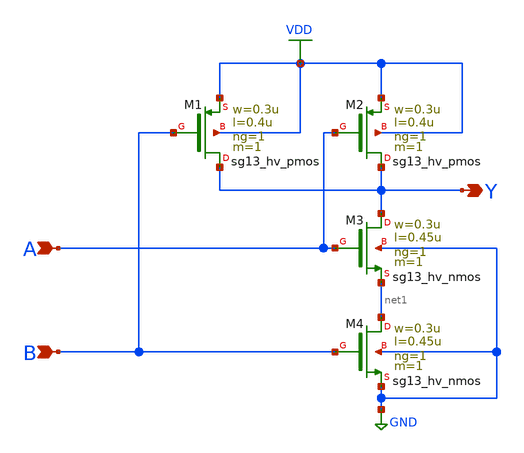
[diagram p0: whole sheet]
** sch_path: 3_real_circuits/nand_gate.sch
**.subckt nand_gate A B Y
*.ipin A
*.ipin B
*.opin Y
XM1 Y B VDD VDD sg13_hv_pmos w=0.3u l=0.4u ng=1 m=1 mm_ok=1
XM2 Y A VDD VDD sg13_hv_pmos w=0.3u l=0.4u ng=1 m=1 mm_ok=1
XM3 Y A net1 GND sg13_hv_nmos w=0.3u l=0.45u ng=1 m=1 mm_ok=1
XM4 net1 B GND GND sg13_hv_nmos w=0.3u l=0.45u ng=1 m=1 mm_ok=1
**.ends
.GLOBAL GND
.GLOBAL VDD
.end
